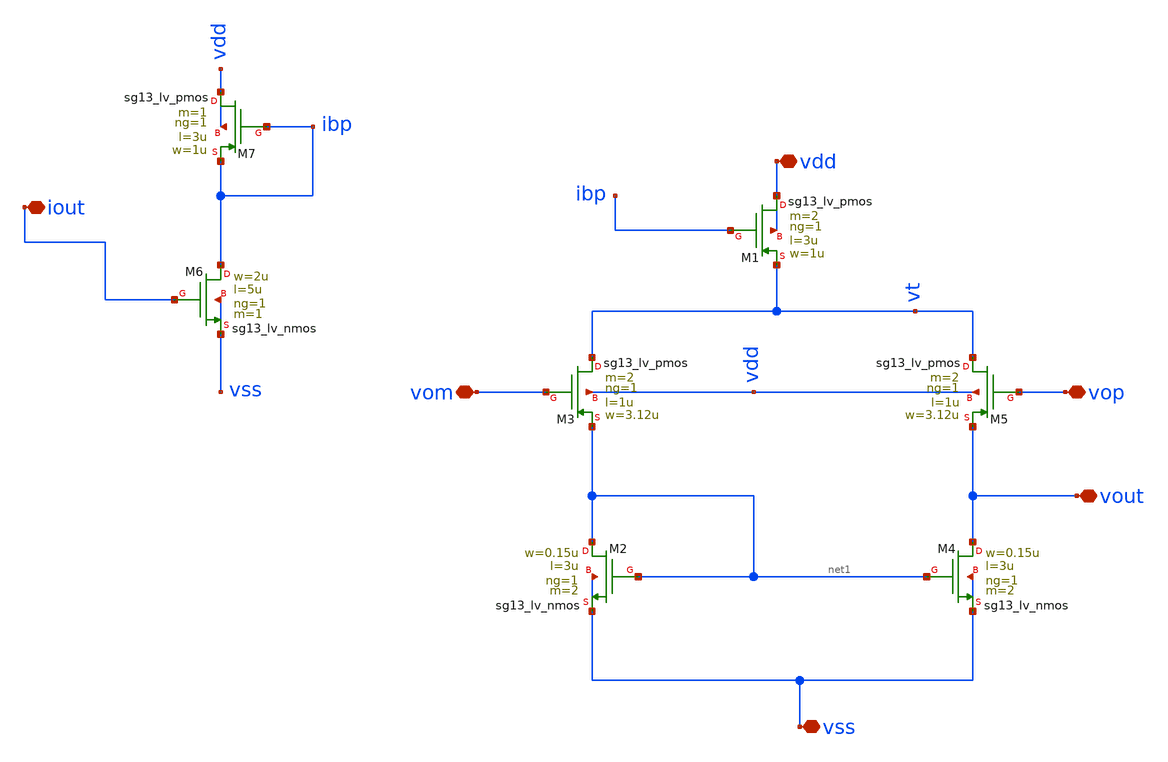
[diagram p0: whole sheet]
** sch_path: schematic/xschem/final_stage_ota/final_stage_ota.sch
**.subckt final_stage_ota vdd vom vop vss vout iout
*.iopin vdd
*.iopin vom
*.iopin vop
*.iopin vss
*.iopin vout
*.iopin iout
XM1 vdd ibp vt vdd sg13_lv_pmos w=1u l=3u ng=1 m=2 mm_ok=1
XM2 net1 net1 vss vss sg13_lv_nmos w=0.15u l=3u ng=1 m=2 mm_ok=1
XM3 vt vom net1 vdd sg13_lv_pmos w=3.12u l=1u ng=1 m=2 mm_ok=1
XM4 vout net1 vss vss sg13_lv_nmos w=0.15u l=3u ng=1 m=2 mm_ok=1
XM5 vt vop vout vdd sg13_lv_pmos w=3.12u l=1u ng=1 m=2 mm_ok=1
XM6 ibp iout vss vss sg13_lv_nmos w=2u l=5u ng=1 m=1 mm_ok=1
XM7 vdd ibp ibp vdd sg13_lv_pmos w=1u l=3u ng=1 m=1 mm_ok=1
**.ends
.end
